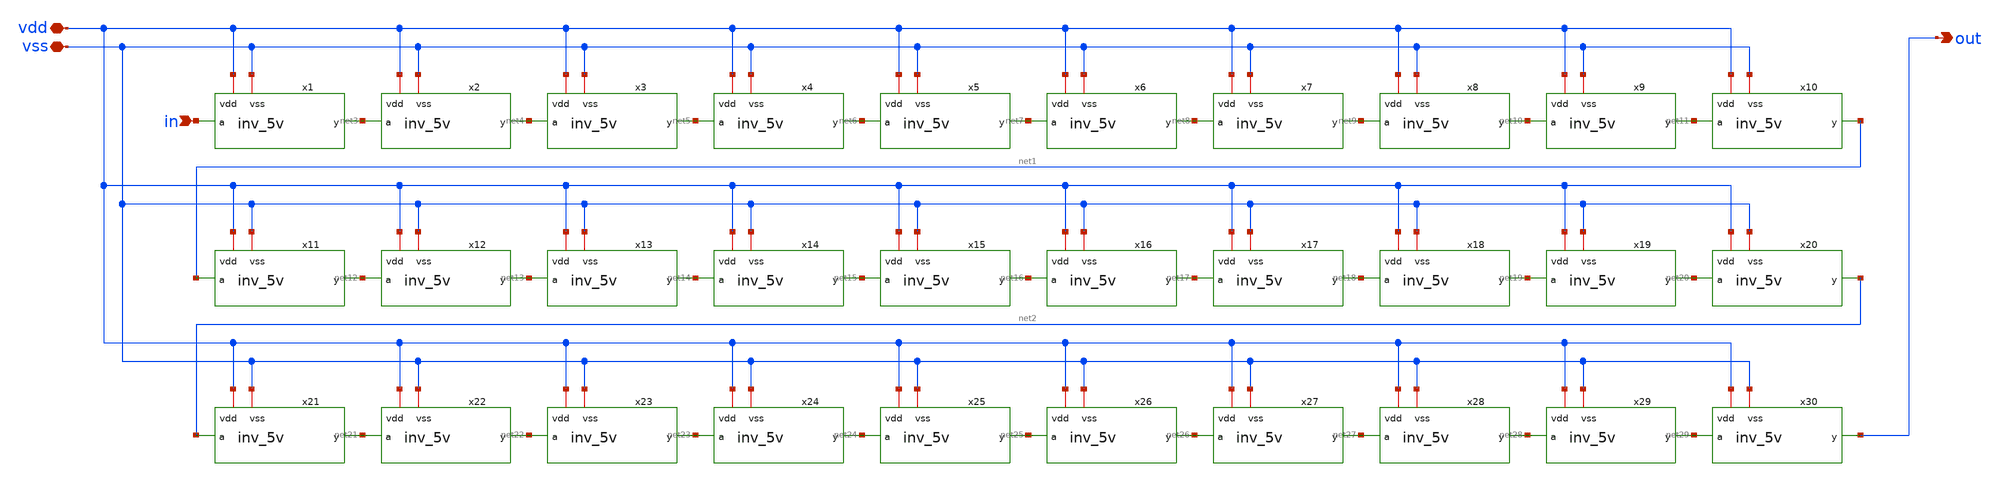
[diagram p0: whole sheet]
** sch_path: member_project/ice458/dynamic_comparator/xschem/delay_5v.sch
**.subckt delay_5v in out vdd vss
*.ipin in
*.opin out
*.iopin vdd
*.iopin vss
x1 vdd in net3 vss inv_5v
x2 vdd net3 net4 vss inv_5v
x3 vdd net4 net5 vss inv_5v
x4 vdd net5 net6 vss inv_5v
x5 vdd net6 net7 vss inv_5v
x6 vdd net7 net8 vss inv_5v
x7 vdd net8 net9 vss inv_5v
x8 vdd net9 net10 vss inv_5v
x9 vdd net10 net11 vss inv_5v
x10 vdd net11 net1 vss inv_5v
x11 vdd net1 net12 vss inv_5v
x12 vdd net12 net13 vss inv_5v
x13 vdd net13 net14 vss inv_5v
x14 vdd net14 net15 vss inv_5v
x15 vdd net15 net16 vss inv_5v
x16 vdd net16 net17 vss inv_5v
x17 vdd net17 net18 vss inv_5v
x18 vdd net18 net19 vss inv_5v
x19 vdd net19 net20 vss inv_5v
x20 vdd net20 net2 vss inv_5v
x21 vdd net2 net21 vss inv_5v
x22 vdd net21 net22 vss inv_5v
x23 vdd net22 net23 vss inv_5v
x24 vdd net23 net24 vss inv_5v
x25 vdd net24 net25 vss inv_5v
x26 vdd net25 net26 vss inv_5v
x27 vdd net26 net27 vss inv_5v
x28 vdd net27 net28 vss inv_5v
x29 vdd net28 net29 vss inv_5v
x30 vdd net29 out vss inv_5v
**.ends

* expanding   symbol:  inv_5v.sym # of pins=4
** sym_path: member_project/ice458/dynamic_comparator/xschem/inv_5v.sym
** sch_path: member_project/ice458/dynamic_comparator/xschem/inv_5v.sch
.subckt inv_5v vdd a y vss
*.iopin vdd
*.iopin vss
*.ipin a
*.opin y
XM3 y a vss vss nfet_06v0 L=0.70u W=1u nf=1 ad='int((nf+1)/2) * W/nf * 0.18u' as='int((nf+2)/2) * W/nf * 0.18u'
+ pd='2*int((nf+1)/2) * (W/nf + 0.18u)' ps='2*int((nf+2)/2) * (W/nf + 0.18u)' nrd='0.18u / W' nrs='0.18u / W'
+ sa=0 sb=0 sd=0 m=1
XM5 y a vdd vdd pfet_05v0 L=0.7u W=3u nf=1 ad='int((nf+1)/2) * W/nf * 0.18u' as='int((nf+2)/2) * W/nf * 0.18u'
+ pd='2*int((nf+1)/2) * (W/nf + 0.18u)' ps='2*int((nf+2)/2) * (W/nf + 0.18u)' nrd='0.18u / W' nrs='0.18u / W'
+ sa=0 sb=0 sd=0 m=1
.ends

.end
